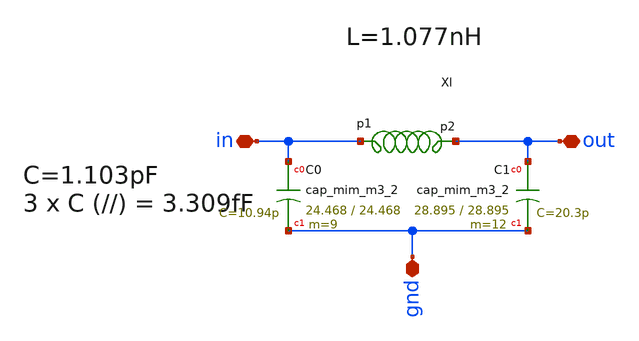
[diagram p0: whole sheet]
** sch_path: impedance-transformer/xschem/impedance-transformer.sch
**.subckt impedance-transformer gnd in out
*.iopin gnd
*.iopin in
*.iopin out
XC0 in gnd sky130_fd_pr__cap_mim_m3_2 W=24.468 L=24.468 MF=9 m=9
XC1 out gnd sky130_fd_pr__cap_mim_m3_2 W=28.895 L=28.895 MF=12 m=12
x1 in out l1
**.ends

* expanding   symbol:  /home/hugodg/projects_sky130/temp_sensor/impedance-transformer/xschem/l1.sym
*+ # of pins=2
** sym_path: impedance-transformer/xschem/l1.sym
** sch_path: impedance-transformer/xschem/l1.sch
.subckt l1 p1 p2
*.iopin p2
*.iopin p1
L0 p1 net3 601.1p m=1
Cs1 p1 net1 47.96f m=1
Cs2 p2 net2 46.2f m=1
Rs1 net1 GND 20.08 m=1
Rs2 net2 GND 15.98 m=1
R1 p2 net3 2.929 m=1
.ends

.GLOBAL GND
.end
